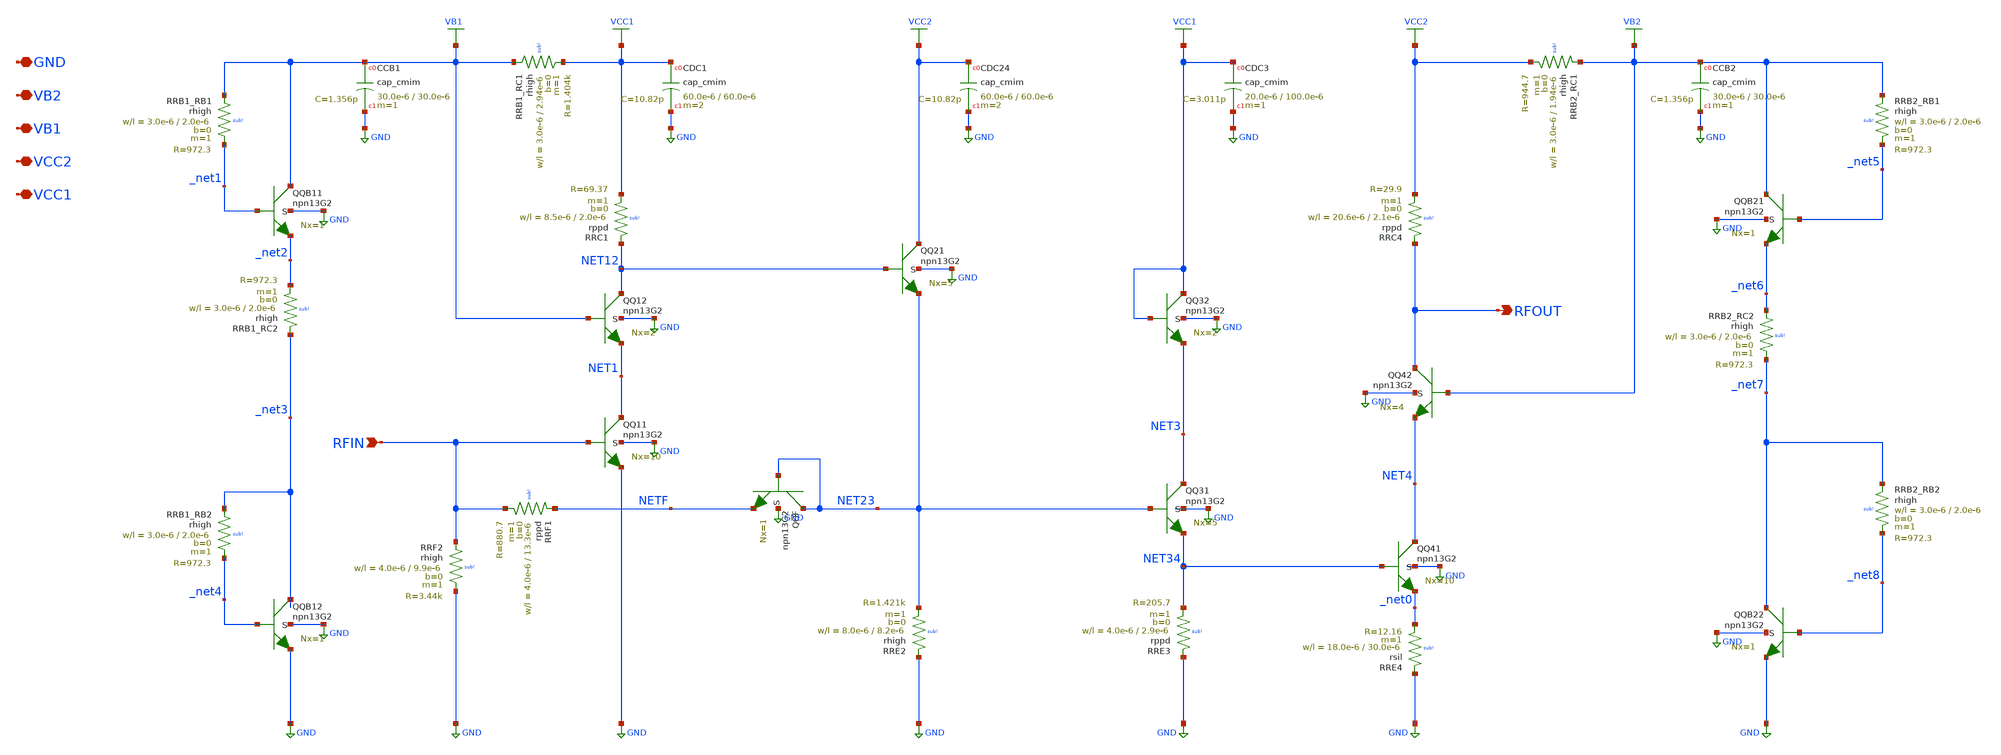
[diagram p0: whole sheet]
** sch_path: TO_Apr2025/97_GHZ_LINEAR_TIA/xschem/97_GHZ_LINEAR_TIA.sch
**.subckt 97_GHZ_LINEAR_TIA RFIN GND VCC1 VCC2 RFOUT VB1 VB2
*.ipin RFIN
*.iopin GND
*.iopin VCC1
*.iopin VCC2
*.opin RFOUT
*.iopin VB1
*.iopin VB2
XQQ11 NET1 RFIN GND GND npn13G2 Nx=10 mm_ok=1
XCDC1 VCC1 GND cap_cmim w=60.0e-6 l=60.0e-6 m=2 mm_ok=1
XQQ21 VCC2 NET12 NET23 GND npn13G2 Nx=5 mm_ok=1
XCDC3 VCC1 GND cap_cmim w=20.0e-6 l=100.0e-6 m=1 mm_ok=1
XRRE2 GND NET23 sub! rhigh w=8.0e-6 l=8.2e-6 m=1 b=0 mm_ok=1
XRRC1 NET12 VCC1 sub! rppd w=8.5e-6 l=2.0e-6 m=1 b=0 mm_ok=1
XQQ31 NET3 NET23 NET34 GND npn13G2 Nx=5 mm_ok=1
XRRF1 NETF RFIN sub! rppd w=4.0e-6 l=13.3e-6 m=1 b=0 mm_ok=1
XRRE3 GND NET34 sub! rppd w=4.0e-6 l=2.9e-6 m=1 b=0 mm_ok=1
XCDC24 VCC2 GND cap_cmim w=60.0e-6 l=60.0e-6 m=2 mm_ok=1
XQQ12 NET12 VB1 NET1 GND npn13G2 Nx=2 mm_ok=1
XRRF2 RFIN GND sub! rhigh w=4.0e-6 l=9.9e-6 m=1 b=0 mm_ok=1
XQQF NET23 NET23 NETF GND npn13G2 Nx=1 mm_ok=1
XQQ32 VCC1 VCC1 NET3 GND npn13G2 Nx=2 mm_ok=1
XQQ41 NET4 NET34 _net0 GND npn13G2 Nx=10 mm_ok=1
XRRE4 GND _net0 sub! rsil w=18.0e-6 l=30.0e-6 m=1 mm_ok=1
XQQ42 RFOUT VB2 NET4 GND npn13G2 Nx=4 mm_ok=1
XRRC4 RFOUT VCC2 sub! rppd w=20.6e-6 l=2.1e-6 m=1 b=0 mm_ok=1
XRRB1_RC1 VB1 VCC1 sub! rhigh w=3.0e-6 l=2.94e-6 m=1 b=0 mm_ok=1
XQQB11 VB1 _net1 _net2 GND npn13G2 Nx=1 mm_ok=1
XRRB1_RB1 VB1 _net1 sub! rhigh w=3.0e-6 l=2.0e-6 m=1 b=0 mm_ok=1
XRRB1_RC2 _net3 _net2 sub! rhigh w=3.0e-6 l=2.0e-6 m=1 b=0 mm_ok=1
XRRB1_RB2 _net3 _net4 sub! rhigh w=3.0e-6 l=2.0e-6 m=1 b=0 mm_ok=1
XQQB12 _net3 _net4 GND GND npn13G2 Nx=1 mm_ok=1
XRRB2_RC1 VB2 VCC2 sub! rhigh w=3.0e-6 l=1.94e-6 m=1 b=0 mm_ok=1
XQQB21 VB2 _net5 _net6 GND npn13G2 Nx=1 mm_ok=1
XRRB2_RB1 VB2 _net5 sub! rhigh w=3.0e-6 l=2.0e-6 m=1 b=0 mm_ok=1
XRRB2_RC2 _net6 _net7 sub! rhigh w=3.0e-6 l=2.0e-6 m=1 b=0 mm_ok=1
XQQB22 _net7 _net8 GND GND npn13G2 Nx=1 mm_ok=1
XRRB2_RB2 _net7 _net8 sub! rhigh w=3.0e-6 l=2.0e-6 m=1 b=0 mm_ok=1
XCCB1 VB1 GND cap_cmim w=30.0e-6 l=30.0e-6 m=1 mm_ok=1
XCCB2 VB2 GND cap_cmim w=30.0e-6 l=30.0e-6 m=1 mm_ok=1
**.ends
.end
